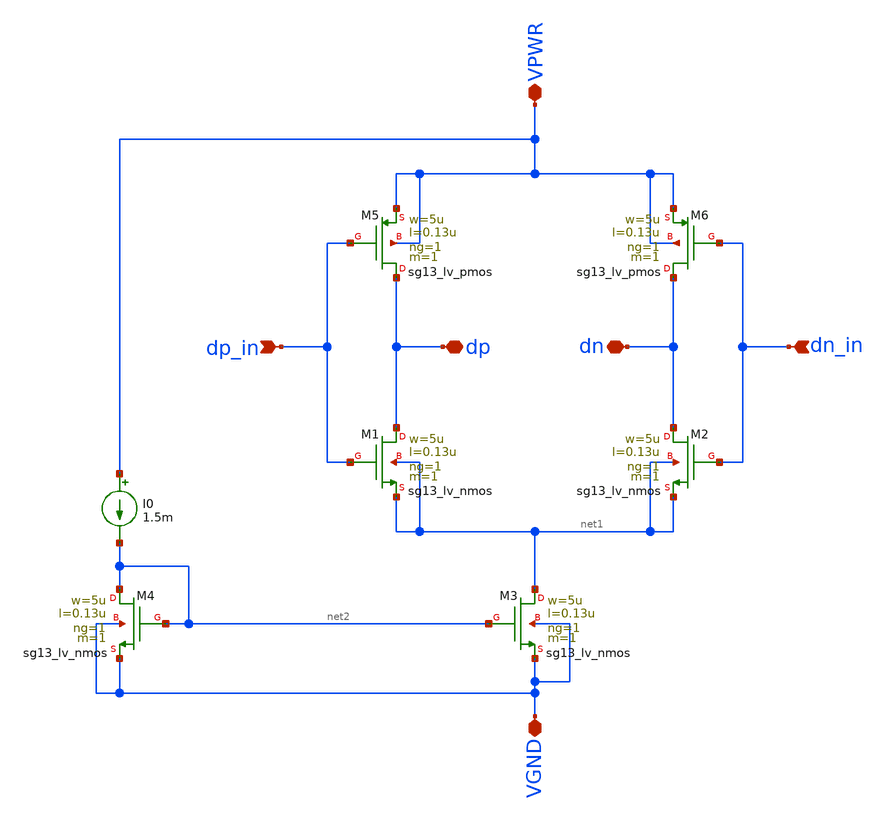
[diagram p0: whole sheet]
** sch_path: xschem/lvds_ideal_mirror.sch
**.subckt lvds_ideal_mirror dp_in dn_in VPWR VGND dp dn
*.ipin dp_in
*.ipin dn_in
*.iopin VPWR
*.iopin VGND
*.iopin dp
*.iopin dn
XM1 dp dp_in net1 net1 sg13_lv_nmos w=5u l=0.13u ng=1 m=1 mm_ok=1
XM2 dn dn_in net1 net1 sg13_lv_nmos w=5u l=0.13u ng=1 m=1 mm_ok=1
XM5 dp dp_in VPWR VPWR sg13_lv_pmos w=5u l=0.13u ng=1 m=1 mm_ok=1
XM6 dn dn_in VPWR VPWR sg13_lv_pmos w=5u l=0.13u ng=1 m=1 mm_ok=1
I0 VPWR net2 1.5m
XM3 net1 net2 VGND VGND sg13_lv_nmos w=5u l=0.13u ng=1 m=1 mm_ok=1
XM4 net2 net2 VGND VGND sg13_lv_nmos w=5u l=0.13u ng=1 m=1 mm_ok=1
**.ends
.end
